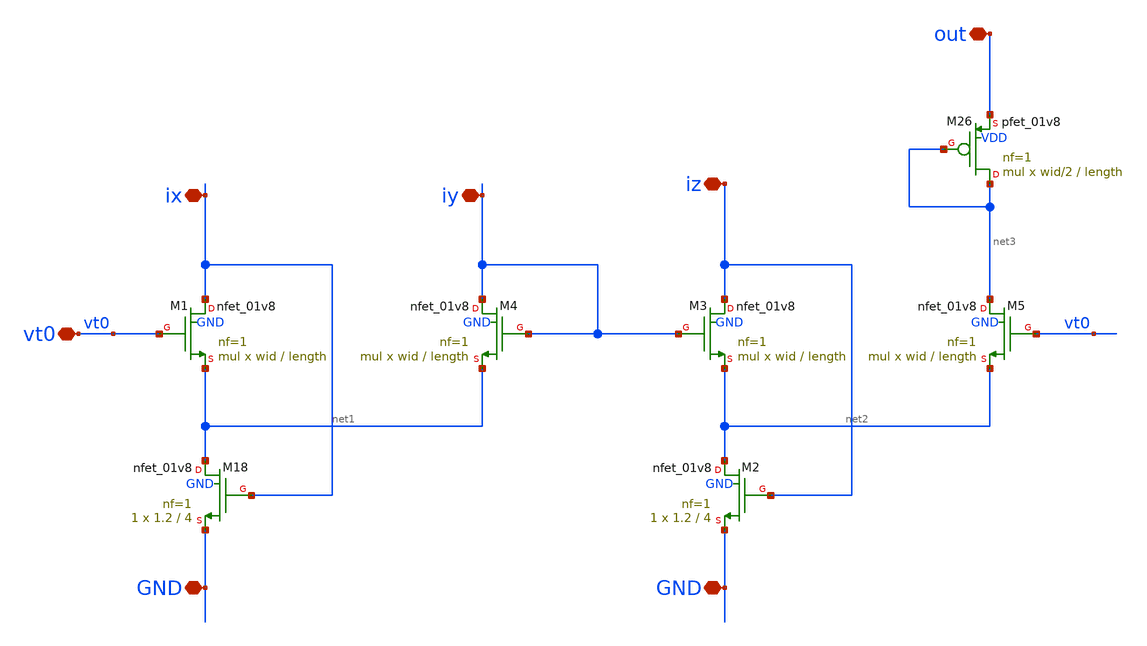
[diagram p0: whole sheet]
** sch_path: xschem/archive/old_blocks/squarer.sch
**.subckt squarer vt0 ix iy iz out GND GND
*.iopin vt0
*.iopin ix
*.iopin iy
*.iopin iz
*.iopin out
*.iopin GND
*.iopin GND
XM18 net1 ix GND GND sky130_fd_pr__nfet_01v8 L=4 W=1.2 nf=1 ad='int((nf+1)/2) * W/nf * 0.29' as='int((nf+2)/2) * W/nf * 0.29'
+ pd='2*int((nf+1)/2) * (W/nf + 0.29)' ps='2*int((nf+2)/2) * (W/nf + 0.29)' nrd='0.29 / W' nrs='0.29 / W'
+ sa=0 sb=0 sd=0 mult=1 m=1
XM1 ix vt0 net1 GND sky130_fd_pr__nfet_01v8 L=length W=wid nf=1 ad='int((nf+1)/2) * W/nf * 0.29' as='int((nf+2)/2) * W/nf * 0.29'
+ pd='2*int((nf+1)/2) * (W/nf + 0.29)' ps='2*int((nf+2)/2) * (W/nf + 0.29)' nrd='0.29 / W' nrs='0.29 / W'
+ sa=0 sb=0 sd=0 mult=mul m=mul
XM2 net2 iz GND GND sky130_fd_pr__nfet_01v8 L=4 W=1.2 nf=1 ad='int((nf+1)/2) * W/nf * 0.29' as='int((nf+2)/2) * W/nf * 0.29'
+ pd='2*int((nf+1)/2) * (W/nf + 0.29)' ps='2*int((nf+2)/2) * (W/nf + 0.29)' nrd='0.29 / W' nrs='0.29 / W'
+ sa=0 sb=0 sd=0 mult=1 m=1
XM3 iz iy net2 GND sky130_fd_pr__nfet_01v8 L=length W=wid nf=1 ad='int((nf+1)/2) * W/nf * 0.29' as='int((nf+2)/2) * W/nf * 0.29'
+ pd='2*int((nf+1)/2) * (W/nf + 0.29)' ps='2*int((nf+2)/2) * (W/nf + 0.29)' nrd='0.29 / W' nrs='0.29 / W'
+ sa=0 sb=0 sd=0 mult=mul m=mul
XM4 iy iy net1 GND sky130_fd_pr__nfet_01v8 L=length W=wid nf=1 ad='int((nf+1)/2) * W/nf * 0.29' as='int((nf+2)/2) * W/nf * 0.29'
+ pd='2*int((nf+1)/2) * (W/nf + 0.29)' ps='2*int((nf+2)/2) * (W/nf + 0.29)' nrd='0.29 / W' nrs='0.29 / W'
+ sa=0 sb=0 sd=0 mult=mul m=mul
XM5 net3 vt0 net2 GND sky130_fd_pr__nfet_01v8 L=length W=wid nf=1 ad='int((nf+1)/2) * W/nf * 0.29' as='int((nf+2)/2) * W/nf * 0.29'
+ pd='2*int((nf+1)/2) * (W/nf + 0.29)' ps='2*int((nf+2)/2) * (W/nf + 0.29)' nrd='0.29 / W' nrs='0.29 / W'
+ sa=0 sb=0 sd=0 mult=mul m=mul
XM26 net3 net3 out VDD sky130_fd_pr__pfet_01v8 L=length W=wid/2 nf=1 ad='int((1 + 1)/2) * wid/2 / 1 * 0.29'
+ as='int((1 + 2)/2) * wid/2 / 1 * 0.29' pd='2*int((1 + 1)/2) * (wid/2 / 1 + 0.29)' ps='2*int((1 + 2)/2) * (wid/2 / 1 + 0.29)'
+ nrd='0.29 / wid/2 ' nrs='0.29 / wid/2 ' sa=0 sb=0 sd=0 mult=mul m=mul
**.ends
.end
